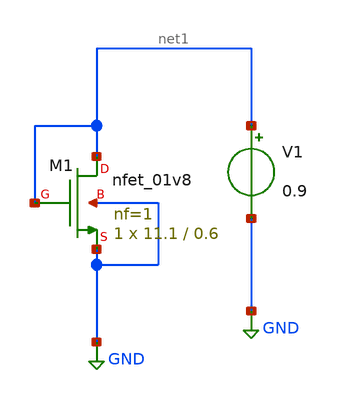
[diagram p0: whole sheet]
** sch_path: BandgapReference/BGR_char.sch
**.subckt BGR_char
XM1 net1 net1 GND GND sky130_fd_pr__nfet_01v8 L=0.6 W=11.1 nf=1 ad='int((nf+1)/2) * W/nf * 0.29' as='int((nf+2)/2) * W/nf * 0.29'
+ pd='2*int((nf+1)/2) * (W/nf + 0.29)' ps='2*int((nf+2)/2) * (W/nf + 0.29)' nrd='0.29 / W' nrs='0.29 / W'
+ sa=0 sb=0 sd=0 mult=1 m=1
V1 net1 GND 0.9
**** begin user architecture code


.include init.txt

.control
save all

save @m.xm1.msky130_fd_pr__nfet_01v8[gm]
save @m.xm1.msky130_fd_pr__nfet_01v8[id]
save @m.xm1.msky130_fd_pr__nfet_01v8[gds]
save @m.xm1.msky130_fd_pr__nfet_01v8[cgg]
save @m.xm1.msky130_fd_pr__nfet_01v8[vdsat]
save @m.xm1.msky130_fd_pr__nfet_01v8[vgs]

dc v1 0 1 1m

let gm = @m.xm1.msky130_fd_pr__nfet_01v8[gm]
let id = @m.xm1.msky130_fd_pr__nfet_01v8[id]
let gds = @m.xm1.msky130_fd_pr__nfet_01v8[gds]
let cgg = @m.xm1.msky130_fd_pr__nfet_01v8[cgg]
let vdsat = @m.xm1.msky130_fd_pr__nfet_01v8[vdsat]
let vgs = @m.xm1.msky130_fd_pr__nfet_01v8[vgs]

let gmro = gm/gds
let ft = gm/(2*pi*cgg)
let gmoverid = gm/id

.endc




**** end user architecture code
**.ends
.GLOBAL GND
.end
